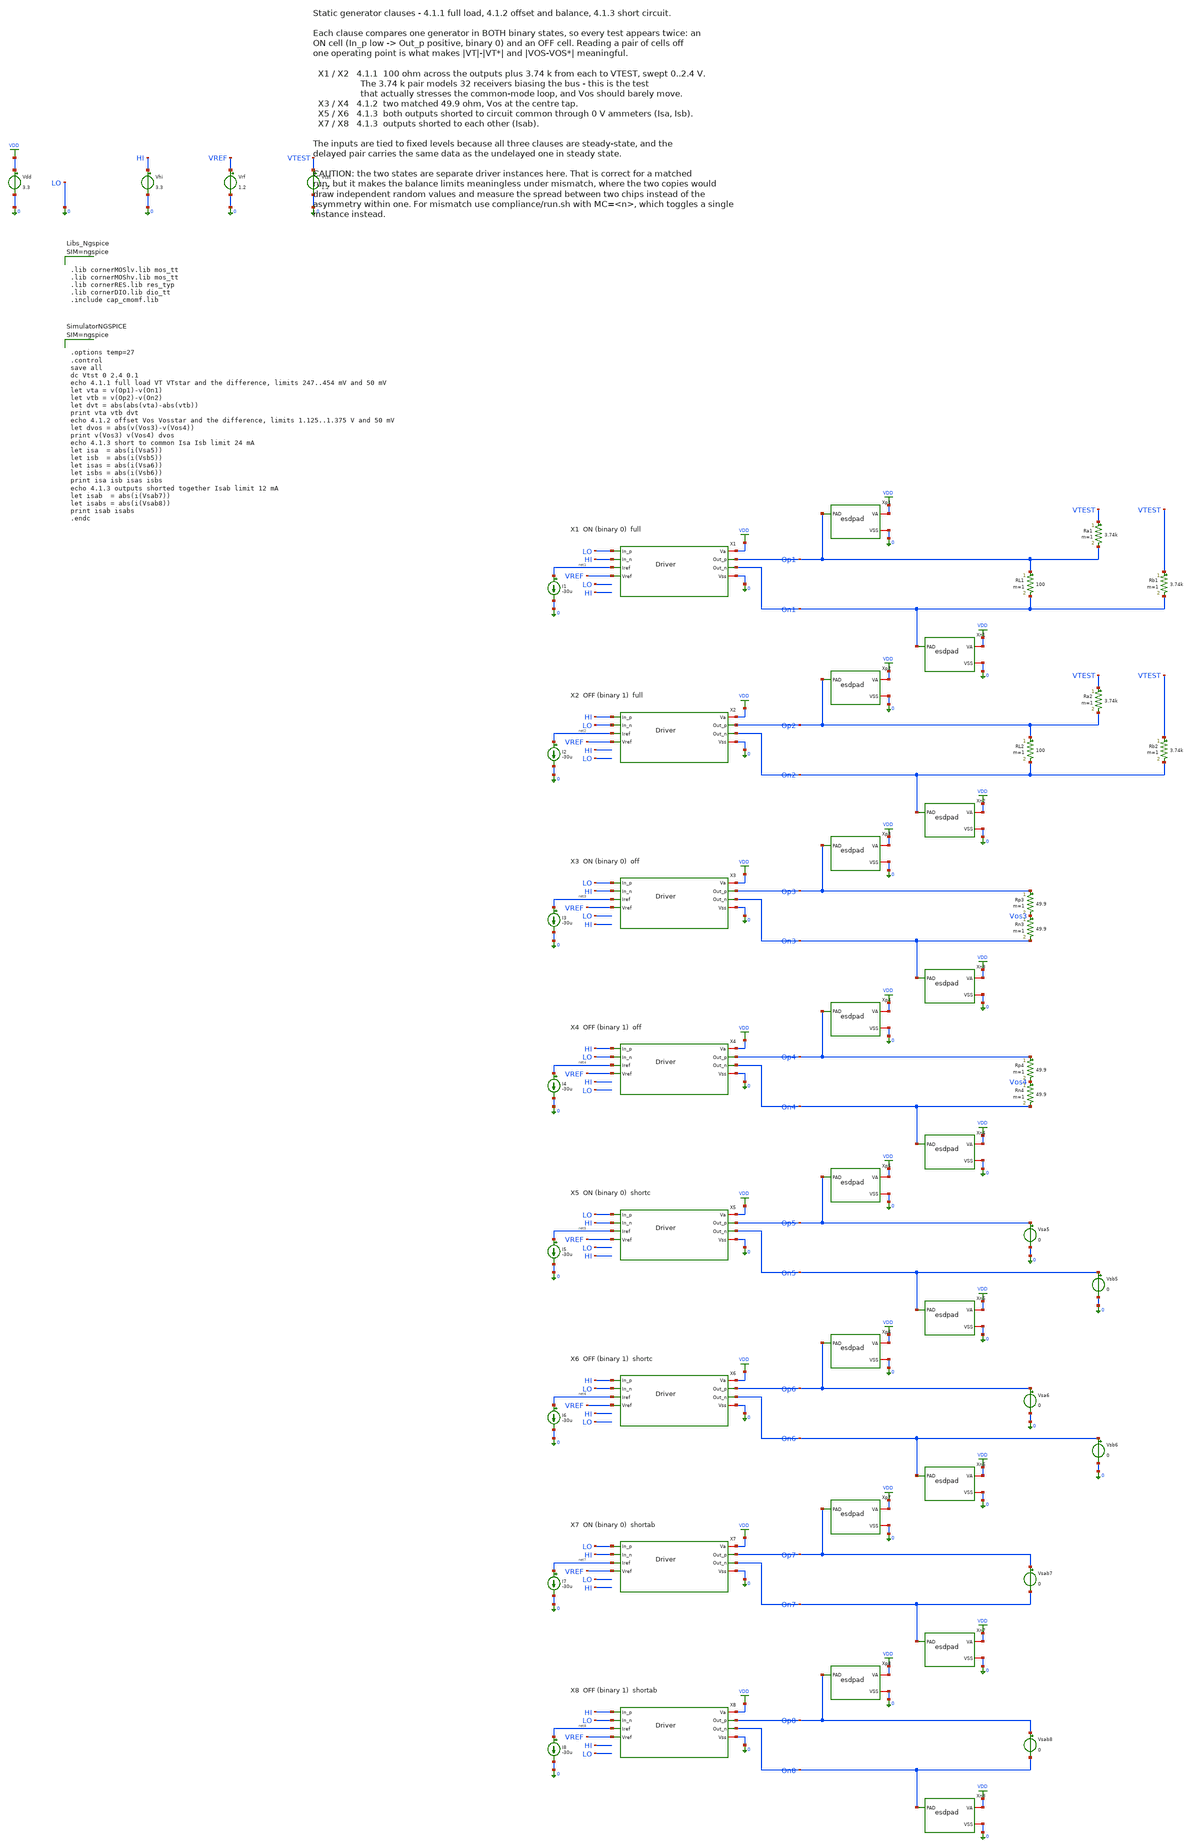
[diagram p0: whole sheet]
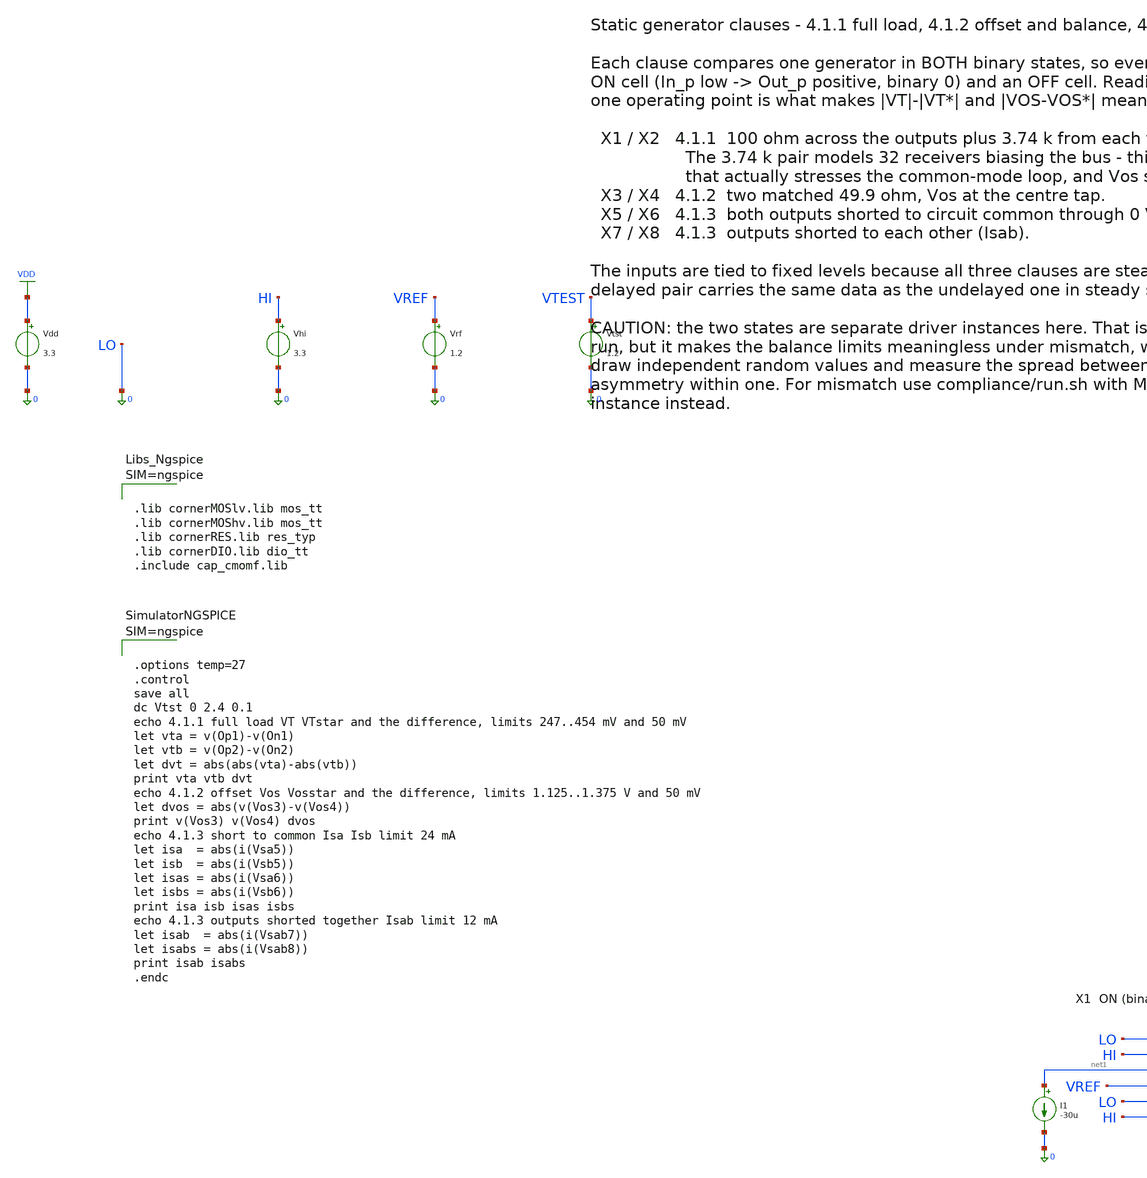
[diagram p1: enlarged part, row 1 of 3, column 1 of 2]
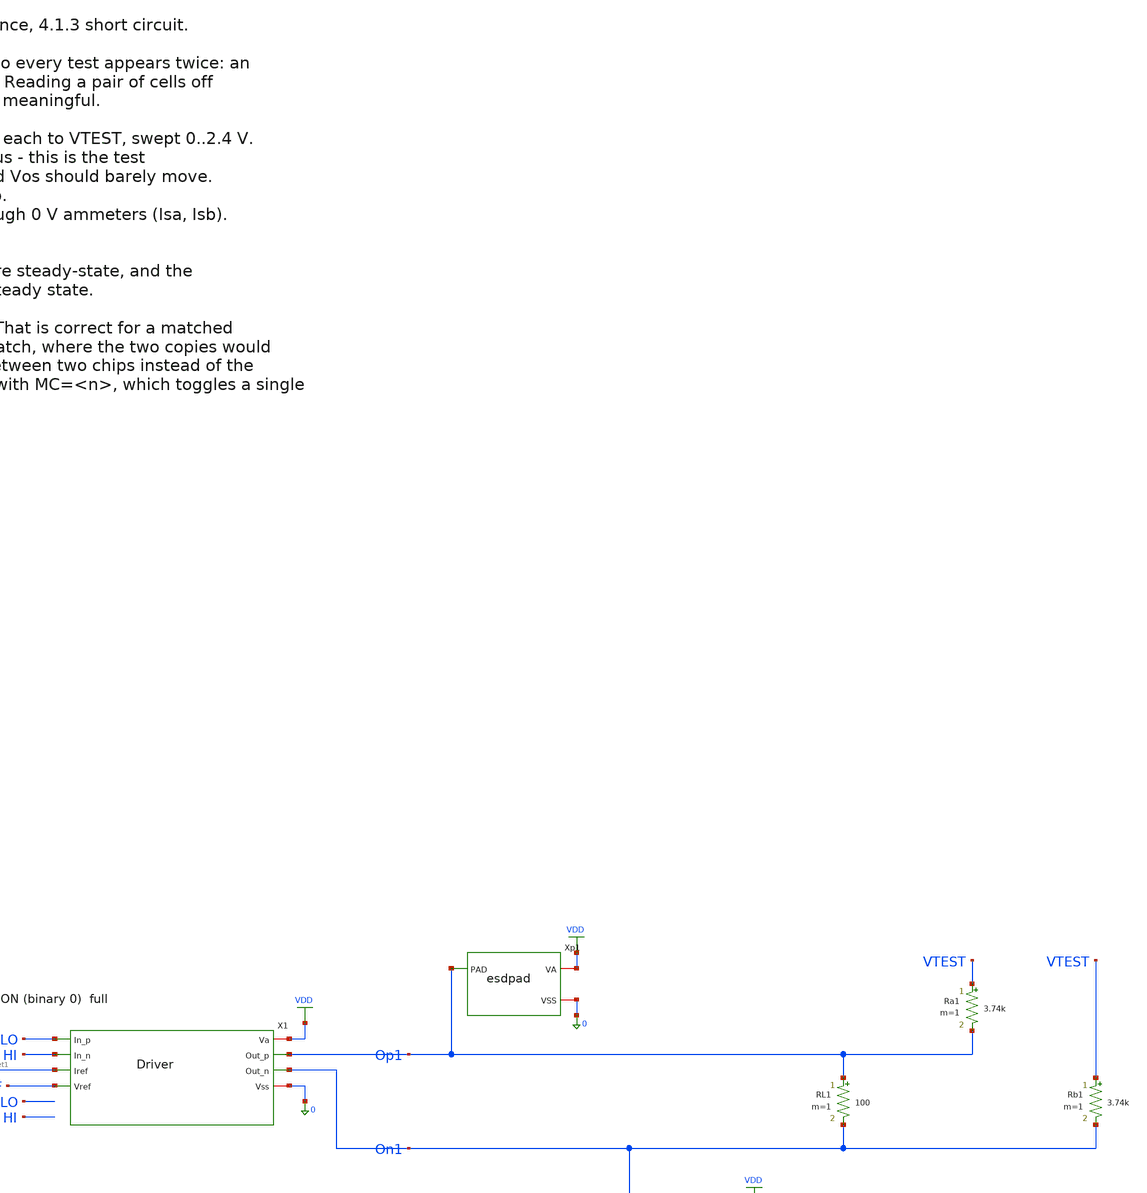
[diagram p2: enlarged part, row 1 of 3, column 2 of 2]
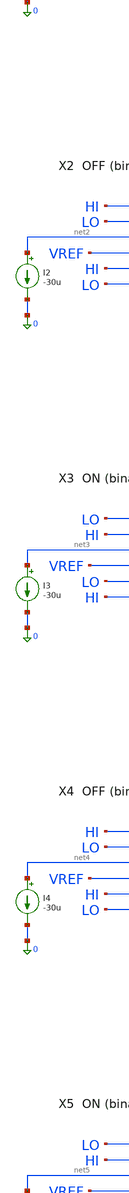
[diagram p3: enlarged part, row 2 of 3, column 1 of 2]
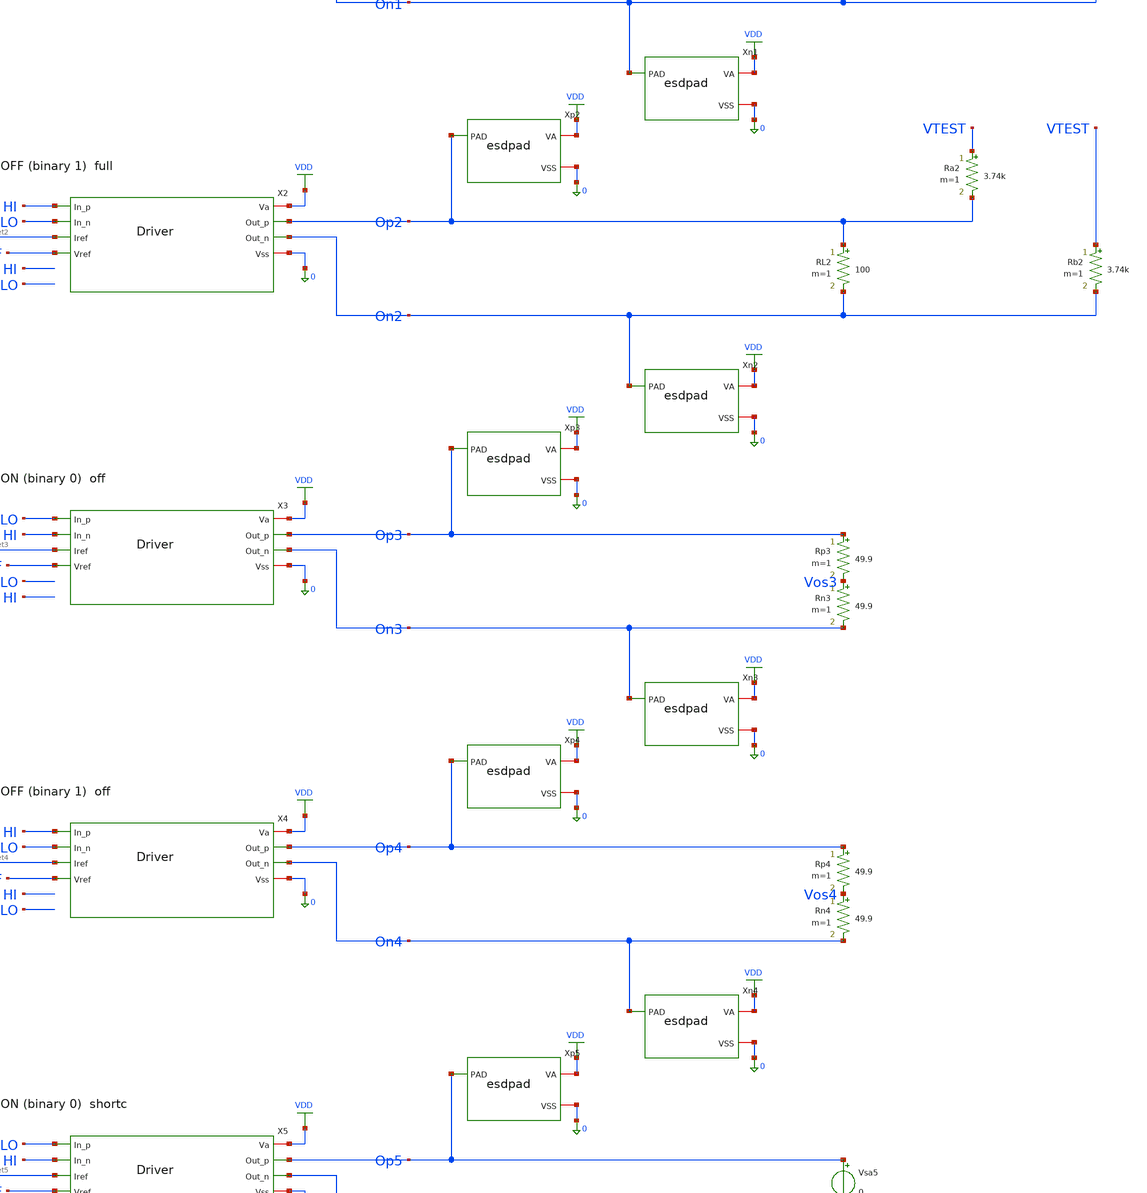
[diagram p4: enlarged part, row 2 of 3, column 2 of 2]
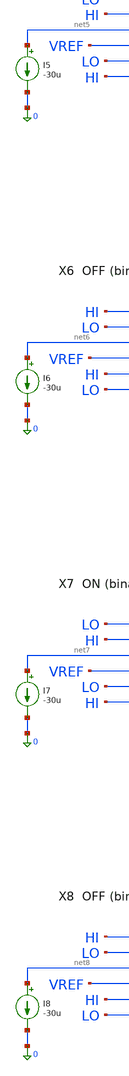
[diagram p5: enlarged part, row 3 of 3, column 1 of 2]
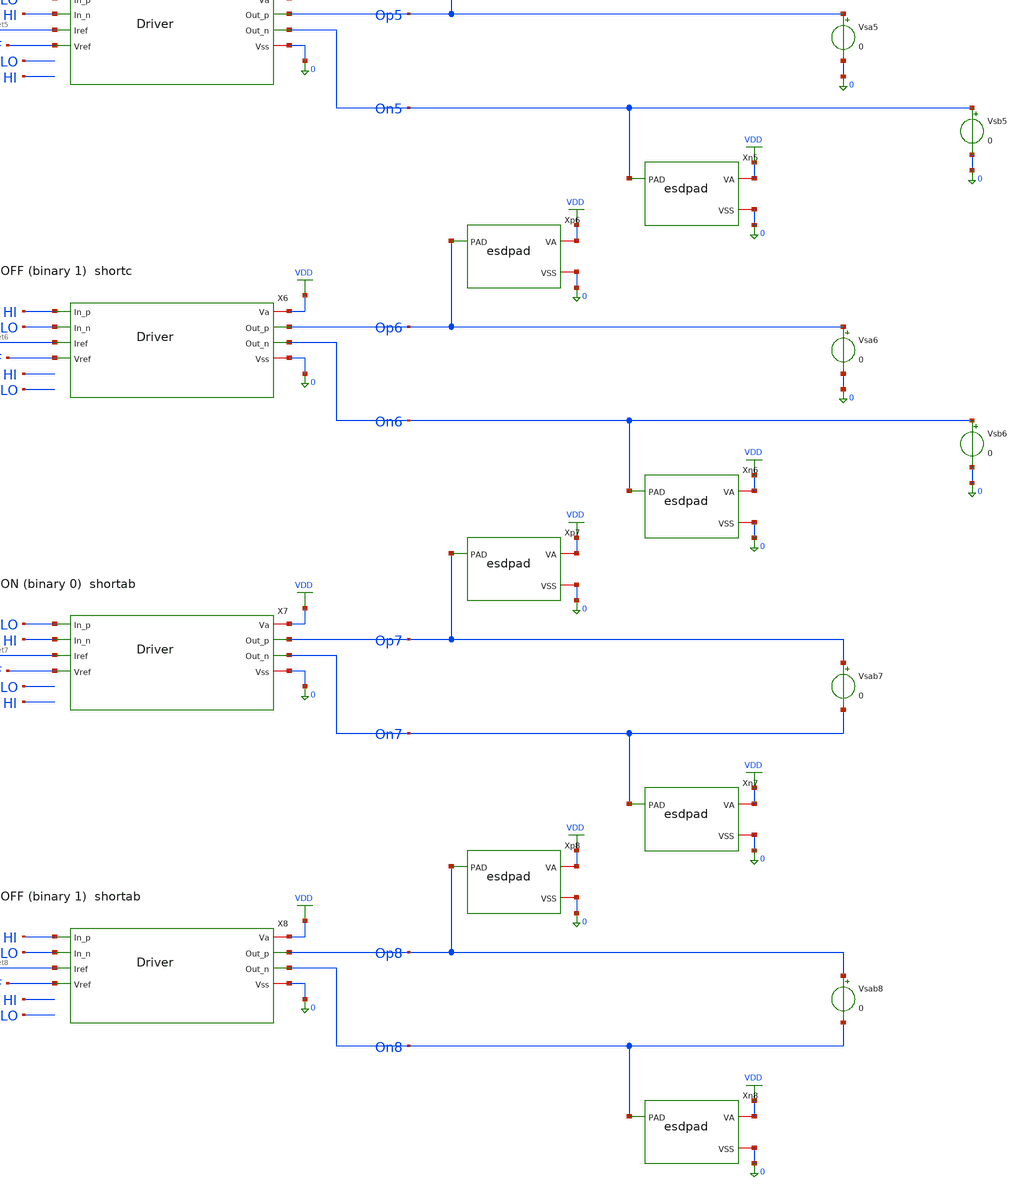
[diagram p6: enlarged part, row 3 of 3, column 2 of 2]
** sch_path: macros/lvds_tx/testbenches/xschem/tb_dc.sch
**.subckt tb_dc
Vdd VDD 0 3.3
Vhi HI 0 3.3
Vrf VREF 0 1.2
Vtst VTEST 0 1.2
X1 VDD Op1 LO HI net1 VREF On1 0 Driver
I1 net1 0 -30u
Xp1 Op1 VDD 0 esdpad
Xn1 On1 VDD 0 esdpad
RL1 Op1 On1 100 m=1
Ra1 VTEST Op1 3.74k m=1
Rb1 VTEST On1 3.74k m=1
X2 VDD Op2 HI LO net2 VREF On2 0 Driver
I2 net2 0 -30u
Xp2 Op2 VDD 0 esdpad
Xn2 On2 VDD 0 esdpad
RL2 Op2 On2 100 m=1
Ra2 VTEST Op2 3.74k m=1
Rb2 VTEST On2 3.74k m=1
X3 VDD Op3 LO HI net3 VREF On3 0 Driver
I3 net3 0 -30u
Xp3 Op3 VDD 0 esdpad
Xn3 On3 VDD 0 esdpad
Rp3 Op3 Vos3 49.9 m=1
Rn3 Vos3 On3 49.9 m=1
X4 VDD Op4 HI LO net4 VREF On4 0 Driver
I4 net4 0 -30u
Xp4 Op4 VDD 0 esdpad
Xn4 On4 VDD 0 esdpad
Rp4 Op4 Vos4 49.9 m=1
Rn4 Vos4 On4 49.9 m=1
X5 VDD Op5 LO HI net5 VREF On5 0 Driver
I5 net5 0 -30u
Xp5 Op5 VDD 0 esdpad
Xn5 On5 VDD 0 esdpad
Vsa5 Op5 0 0
.save i(vsa5)
Vsb5 On5 0 0
.save i(vsb5)
X6 VDD Op6 HI LO net6 VREF On6 0 Driver
I6 net6 0 -30u
Xp6 Op6 VDD 0 esdpad
Xn6 On6 VDD 0 esdpad
Vsa6 Op6 0 0
.save i(vsa6)
Vsb6 On6 0 0
.save i(vsb6)
X7 VDD Op7 LO HI net7 VREF On7 0 Driver
I7 net7 0 -30u
Xp7 Op7 VDD 0 esdpad
Xn7 On7 VDD 0 esdpad
Vsab7 Op7 On7 0
.save i(vsab7)
X8 VDD Op8 HI LO net8 VREF On8 0 Driver
I8 net8 0 -30u
Xp8 Op8 VDD 0 esdpad
Xn8 On8 VDD 0 esdpad
Vsab8 Op8 On8 0
.save i(vsab8)
**** begin user architecture code



.lib cornerMOSlv.lib mos_tt
.lib cornerMOShv.lib mos_tt
.lib cornerRES.lib res_typ
.lib cornerDIO.lib dio_tt
.include cap_cmomf.lib






.options temp=27
.control
save all
dc Vtst 0 2.4 0.1
echo 4.1.1 full load VT VTstar and the difference, limits 247..454 mV and 50 mV
let vta = v(Op1)-v(On1)
let vtb = v(Op2)-v(On2)
let dvt = abs(abs(vta)-abs(vtb))
print vta vtb dvt
echo 4.1.2 offset Vos Vosstar and the difference, limits 1.125..1.375 V and 50 mV
let dvos = abs(v(Vos3)-v(Vos4))
print v(Vos3) v(Vos4) dvos
echo 4.1.3 short to common Isa Isb limit 24 mA
let isa  = abs(i(Vsa5))
let isb  = abs(i(Vsb5))
let isas = abs(i(Vsa6))
let isbs = abs(i(Vsb6))
print isa isb isas isbs
echo 4.1.3 outputs shorted together Isab limit 12 mA
let isab  = abs(i(Vsab7))
let isabs = abs(i(Vsab8))
print isab isabs
.endc



**** end user architecture code
**.ends

* expanding   symbol:  Driver.sym # of pins=8
** sym_path: macros/lvds_tx/schematic/xschem/Driver.sym
** sch_path: macros/lvds_tx/schematic/xschem/Driver.sch
.subckt Driver Va Out_p In_p In_n Iref Vref Out_n Vss
*.iopin Va
*.iopin Vss
*.opin Out_p
*.opin Out_n
*.ipin In_p
*.ipin In_n
*.ipin Iref
*.ipin Vref
XCtn1 Va tail_n Va Va sg13_hv_pmos w=11.8u l=5.25u ng=2 m=1 mm_ok=1
XCtn2 Va tail_n Va Va sg13_hv_pmos w=5.7u l=5.8u ng=2 m=1 mm_ok=1
XM2 tail_p cmfb Va Va sg13_hv_pmos w=97.2u l=0.5u ng=20 m=1 mm_ok=1
XM5 Out_p In_p tail_p Va sg13_hv_pmos w=80u l=0.4u ng=16 m=1 mm_ok=1
XM4 Out_n In_n tail_p Va sg13_hv_pmos w=80u l=0.4u ng=16 m=1 mm_ok=1
XM1 Out_p In_p tail_n Vss sg13_hv_nmos w=30u l=0.45u ng=15 m=1 mm_ok=1
XM3 Out_n In_n tail_n Vss sg13_hv_nmos w=30u l=0.45u ng=15 m=1 mm_ok=1
XM6 tail_n Iref Vss Vss sg13_hv_nmos w=49.6u l=0.5u ng=31 m=2 mm_ok=1
XM9 Iref Iref Vss Vss sg13_hv_nmos w=0.8u l=0.5u ng=1 m=1 mm_ok=1
XM13 pd pd Va Va sg13_hv_pmos w=5u l=1u ng=1 m=1 mm_ok=1
XM14 cmfb pd Va Va sg13_hv_pmos w=5u l=1u ng=1 m=1 mm_ok=1
XM11 pd cm otail Vss sg13_hv_nmos w=40u l=1u ng=16 m=1 mm_ok=1
XM12 cmfb Vref otail Vss sg13_hv_nmos w=40u l=1u ng=16 m=1 mm_ok=1
XM10 otail Iref Vss Vss sg13_hv_nmos w=0.8u l=0.5u ng=1 m=1 mm_ok=1
XCc Va cc_g Va Va sg13_hv_pmos w=50u l=5u ng=10 m=1 mm_ok=1
XRc cmfb cc_g Vss rppd w=1u l=6u m=1 b=0 mm_ok=1
XRp Out_p cm Vss rhigh w=1u l=7.35u m=1 b=0 mm_ok=1
XRn Out_n cm Vss rhigh w=1u l=7.35u m=1 b=0 mm_ok=1
XCxp Out_p In_n cap_cmomf w=5.913u l=5.913u mmin=1 mmax=4 subblock=0 rfmodel=0 subscale=1 m=1
+ mm_ok=1
XCxn Out_n In_p cap_cmomf w=5.913u l=5.913u mmin=1 mmax=4 subblock=0 rfmodel=0 subscale=1 m=1
+ mm_ok=1
XCop Vss Out_p Vss Vss sg13_hv_nmos w=10u l=5u ng=1 m=2 mm_ok=1
XCon Vss Out_n Vss Vss sg13_hv_nmos w=10u l=5u ng=1 m=2 mm_ok=1
.ends


* expanding   symbol:  esdpad.sym # of pins=3
** sym_path: macros/lvds_tx/schematic/xschem/esdpad.sym
** sch_path: macros/lvds_tx/schematic/xschem/esdpad.sch
.subckt esdpad PAD VA VSS
*.iopin PAD
*.iopin VA
*.iopin VSS
XDdvdd VA PAD VSS diodevdd_4kv m=1
XDdvss VA PAD VSS diodevss_4kv m=1
Cpad PAD VSS 90f m=1
.ends

.GLOBAL VDD
.end
